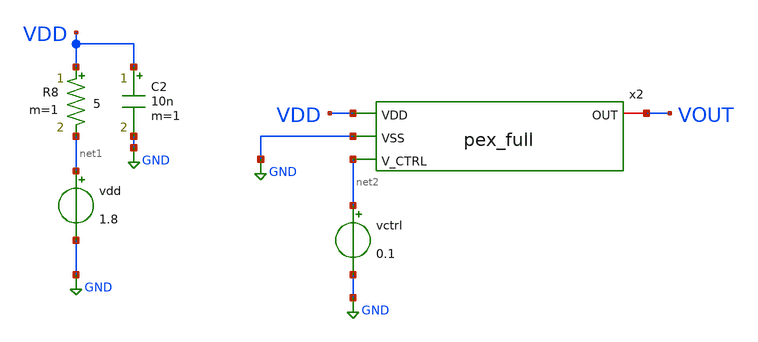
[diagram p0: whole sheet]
** sch_path: schem/jit_full_tb.sch
**.subckt jit_full_tb
vdd net1 GND 1.8
C2 VDD GND 10n m=1
R8 VDD net1 5 m=1
vctrl net2 GND 0.1
x2 VDD GND VOUT net2 vco_pex
**** begin user architecture code


.include /home/zhixuan/projects/fyp_vco/magic/full/vco_pex.spice
.lib /usr/local/share/pdk/sky130A/libs.tech/ngspice/sky130.lib.spice tt
.save all

.control
    tran 0.1n 100u

    * Find all rising edge crossings at 0.9V
    * meas repeated with rising index to capture every cycle
    let n = 2
    let max_cycles = 150
    let done = 0

    echo "edge,time_s" > /home/zhixuan/projects/fyp_vco/schem/jitter_out.csv

    dowhile done < 1
        meas tran t_edge when VOUT=0.9 rise=n
        if t_edge > 0
            echo "$&n,$&t_edge" >> /home/zhixuan/projects/fyp_vco/schem/jitter_out.csv
            let n = n + 1
            if n > max_cycles
                let done = 1
            end
        else
            let done = 1
        end
    end

.endc

.end


**** end user architecture code
**.ends
.GLOBAL GND
.end
